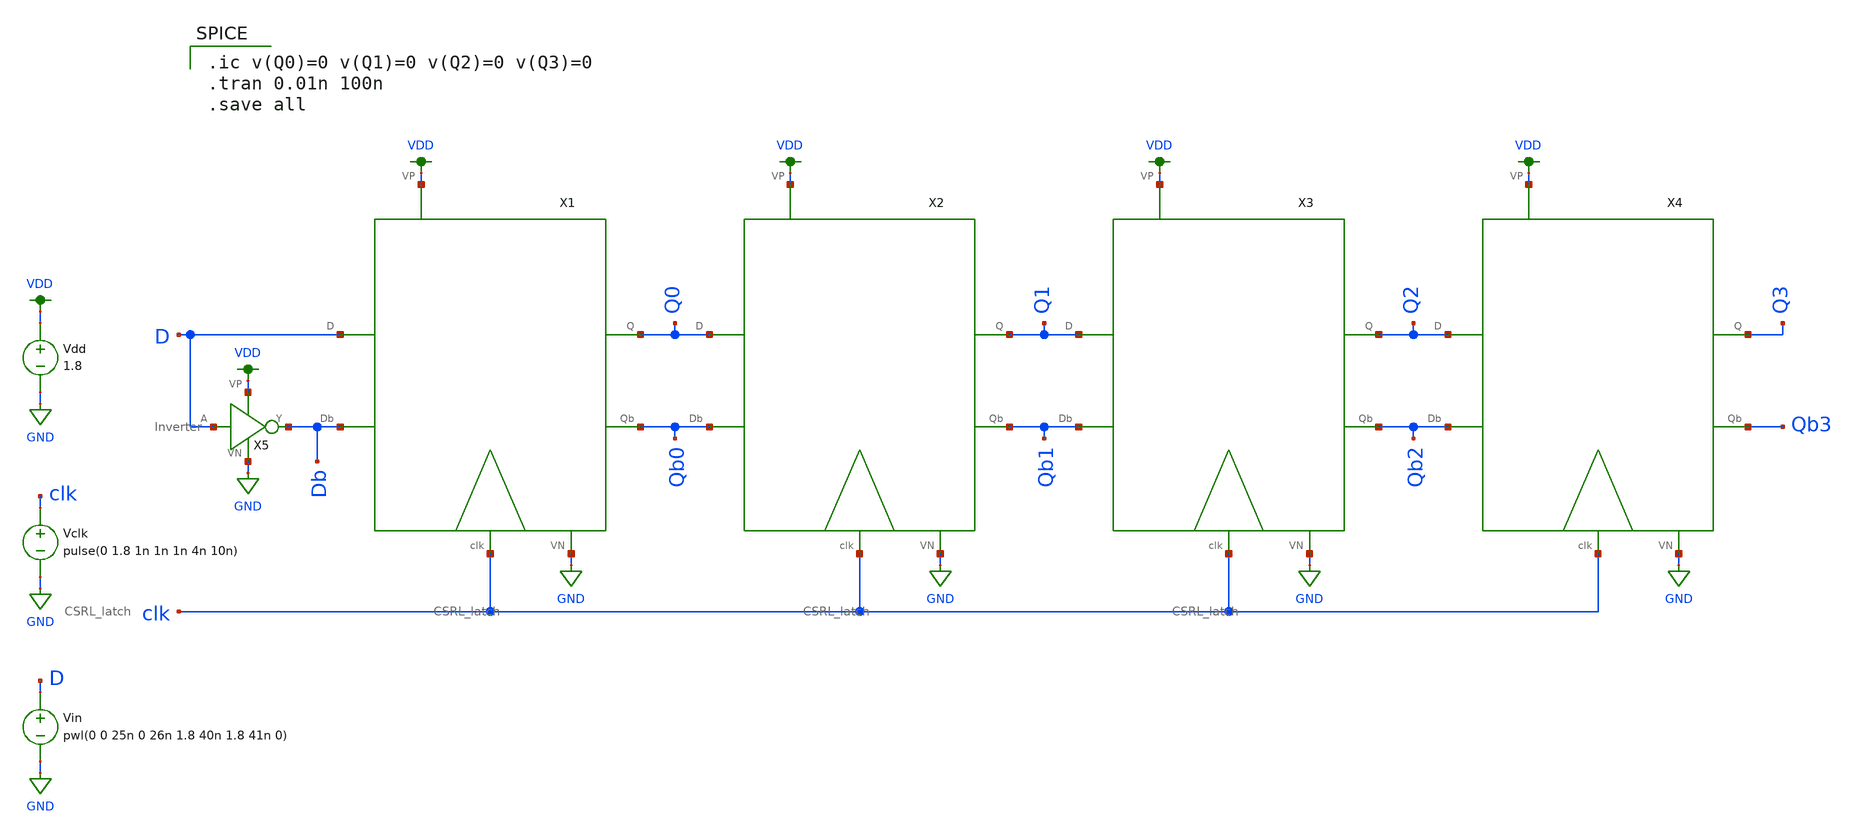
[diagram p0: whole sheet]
** sch_path: Mini_Project_2/Shift_reg/schematics/Shift_reg_simulation.sch
**.subckt Shift_reg_simulation
X1 D Db Q0 Qb0 VDD clk GND CSRL_latch
X2 Q0 Qb0 Q1 Qb1 VDD clk GND CSRL_latch
X5 D Db VDD GND Inverter
X3 Q1 Qb1 Q2 Qb2 VDD clk GND CSRL_latch
X4 Q2 Qb2 Q3 Qb3 VDD clk GND CSRL_latch
Vdd VDD GND 1.8
Vclk clk GND pulse(0 1.8 1n 1n 1n 4n 10n)
Vin D GND pwl(0 0 25n 0 26n 1.8 40n 1.8 41n 0)
**** begin user architecture code

.ic v(Q0)=0 v(Q1)=0 v(Q2)=0 v(Q3)=0
.tran 0.01n 100n
.save all


.option wnflag=1
.lib ~/skywater/skywater-pdk/libraries/sky130_fd_pr_ngspice/latest/models/sky130.lib.spice tt

**** end user architecture code
**.ends
.GLOBAL VDD
.GLOBAL GND
.end
